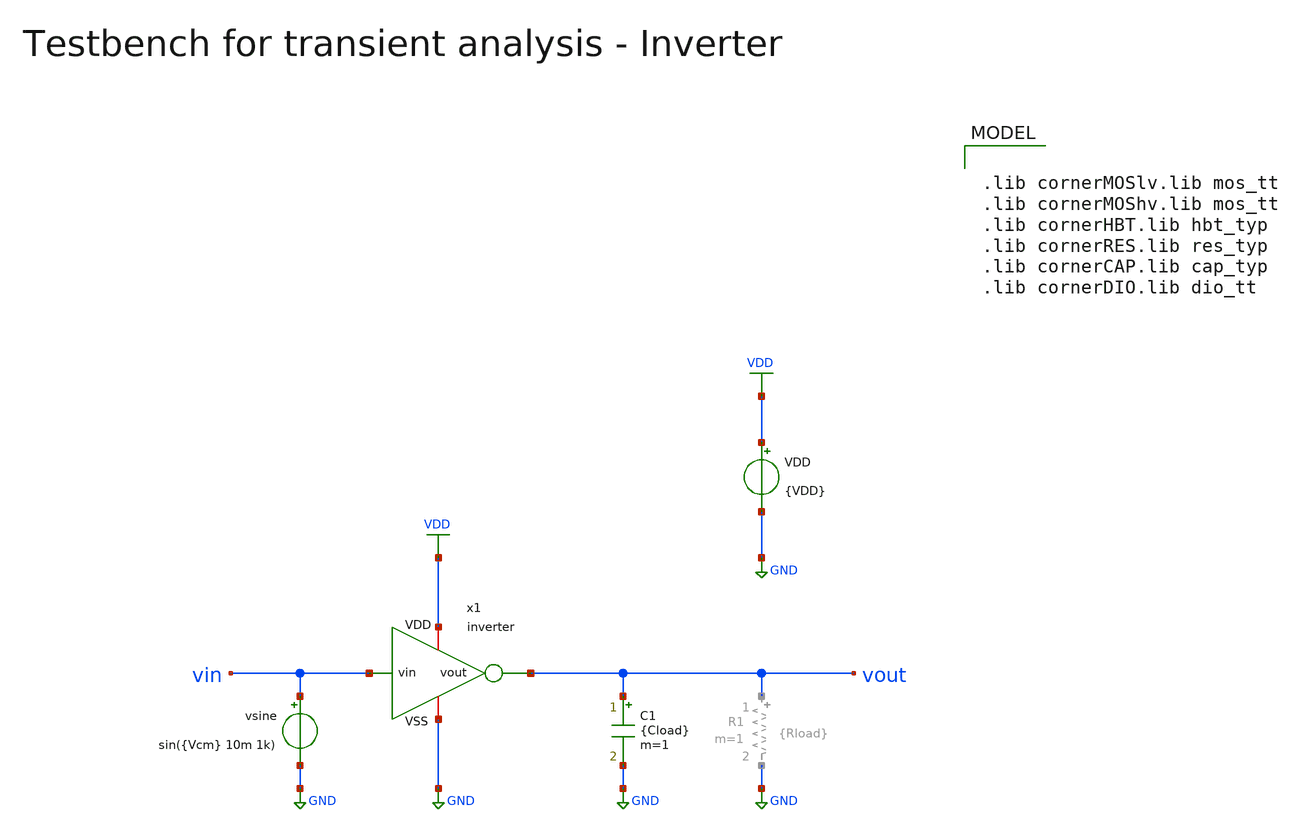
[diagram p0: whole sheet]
** sch_path: macros/inverter/testbenches/xschem/inverter_tb_tran.sch
**.subckt inverter_tb_tran
VDD VDD GND {VDD}
vsine vin GND sin({Vcm} 10m 1k)
C1 vout GND {Cload} m=1
x1 VDD vin vout GND inverter
**** begin user architecture code


.param VDD=1.5
.csparam VDD=VDD
.param Vcm=VDD/2
.param temp=27
.param Cload=10p
.param Rload=1k
.options savecurrents klu method=gear reltol=1e-4 abstol=1e-15 gmin=1e-15
.control

save all

* Operating Point Analysis
op
remzerovec
write @schname\.raw
set appendwrite

* Transient Analysis
tran 1u 5m
write @schname\.raw

* Plotting
plot vin vout
plot i(VDD)

* Measurements
meas tran vin_peak MAX v(vin)
meas tran vout_peak MAX v(vout)

let Adm = vout_peak / vin_peak
let Adm_dB = vdb(Adm)
print Adm_dB

meas tran vout_pp_max MAX v(vout)
meas tran vout_pp_min MIN v(vout)
let vout_pp = vout_pp_max - vout_pp_min
print vout_pp

* Write Data
unset appendwrite
set wr_vecnames
set wr_singlescale
wrdata ../../../scripts/plot_simulations/data/@schname\.txt v(vin) v(vout)

*quit
.endc



.lib cornerMOSlv.lib mos_tt
.lib cornerMOShv.lib mos_tt
.lib cornerHBT.lib hbt_typ
.lib cornerRES.lib res_typ
.lib cornerCAP.lib cap_typ
.lib cornerDIO.lib dio_tt

**** end user architecture code
**.ends
.GLOBAL GND
.GLOBAL VDD
.end
